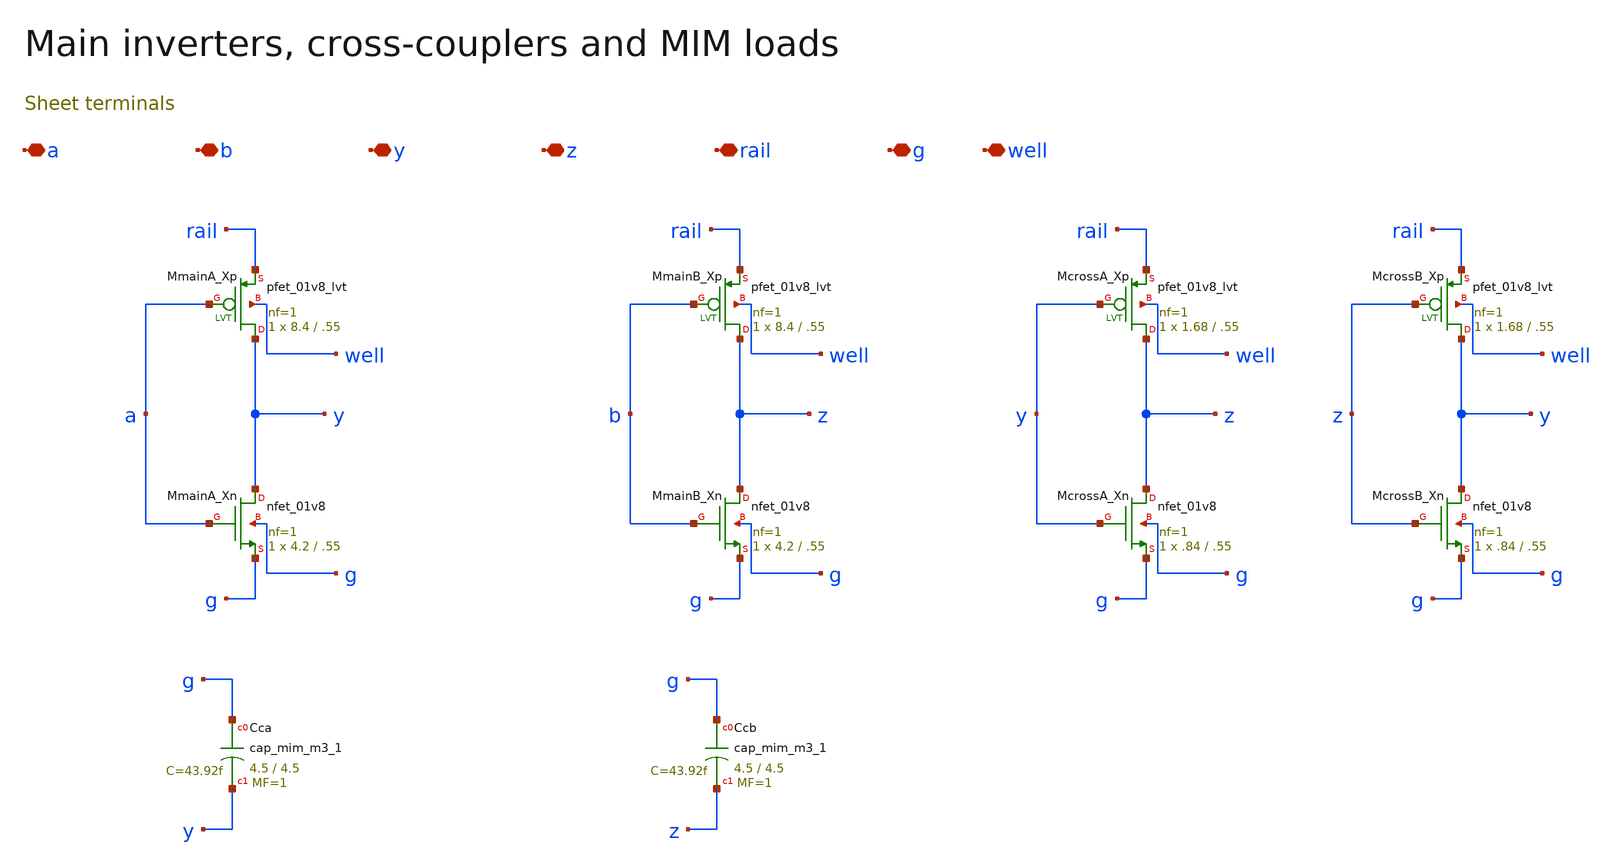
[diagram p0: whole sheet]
** sch_path: review/xschem/stage.sch
**.subckt stage a b y z rail g well
*.iopin a
*.iopin b
*.iopin y
*.iopin z
*.iopin rail
*.iopin g
*.iopin well
XCca g y sky130_fd_pr__cap_mim_m3_1 W=4.5 L=4.5 MF=1 m=1
XCcb g z sky130_fd_pr__cap_mim_m3_1 W=4.5 L=4.5 MF=1 m=1
XMmainA_Xp y a rail well sky130_fd_pr__pfet_01v8_lvt L=.55 W=8.4 nf=1 ad='int((1 + 1)/2) * 8.4 / 1 * 0.29'
+ as='int((1 + 2)/2) * 8.4 / 1 * 0.29' pd='2*int((1 + 1)/2) * (8.4 / 1 + 0.29)' ps='2*int((1 + 2)/2) * (8.4 / 1 + 0.29)'
+ nrd='0.29 / 8.4 ' nrs='0.29 / 8.4 ' sa=0 sb=0 sd=0 mult=1 m=1
XMmainA_Xn y a g g sky130_fd_pr__nfet_01v8 L=.55 W=4.2 nf=1 ad='int((1 + 1)/2) * 4.2 / 1 * 0.29' as='int((1 + 2)/2) * 4.2 / 1 * 0.29'
+ pd='2*int((1 + 1)/2) * (4.2 / 1 + 0.29)' ps='2*int((1 + 2)/2) * (4.2 / 1 + 0.29)' nrd='0.29 / 4.2 ' nrs='0.29 / 4.2 '
+ sa=0 sb=0 sd=0 mult=1 m=1
XMmainB_Xp z b rail well sky130_fd_pr__pfet_01v8_lvt L=.55 W=8.4 nf=1 ad='int((1 + 1)/2) * 8.4 / 1 * 0.29'
+ as='int((1 + 2)/2) * 8.4 / 1 * 0.29' pd='2*int((1 + 1)/2) * (8.4 / 1 + 0.29)' ps='2*int((1 + 2)/2) * (8.4 / 1 + 0.29)'
+ nrd='0.29 / 8.4 ' nrs='0.29 / 8.4 ' sa=0 sb=0 sd=0 mult=1 m=1
XMmainB_Xn z b g g sky130_fd_pr__nfet_01v8 L=.55 W=4.2 nf=1 ad='int((1 + 1)/2) * 4.2 / 1 * 0.29' as='int((1 + 2)/2) * 4.2 / 1 * 0.29'
+ pd='2*int((1 + 1)/2) * (4.2 / 1 + 0.29)' ps='2*int((1 + 2)/2) * (4.2 / 1 + 0.29)' nrd='0.29 / 4.2 ' nrs='0.29 / 4.2 '
+ sa=0 sb=0 sd=0 mult=1 m=1
XMcrossA_Xp z y rail well sky130_fd_pr__pfet_01v8_lvt L=.55 W=1.68 nf=1 ad='int((1 + 1)/2) * 1.68 / 1 * 0.29'
+ as='int((1 + 2)/2) * 1.68 / 1 * 0.29' pd='2*int((1 + 1)/2) * (1.68 / 1 + 0.29)' ps='2*int((1 + 2)/2) * (1.68 / 1 + 0.29)'
+ nrd='0.29 / 1.68 ' nrs='0.29 / 1.68 ' sa=0 sb=0 sd=0 mult=1 m=1
XMcrossA_Xn z y g g sky130_fd_pr__nfet_01v8 L=.55 W=.84 nf=1 ad='int((1 + 1)/2) * .84 / 1 * 0.29' as='int((1 + 2)/2) * .84 / 1 * 0.29'
+ pd='2*int((1 + 1)/2) * (.84 / 1 + 0.29)' ps='2*int((1 + 2)/2) * (.84 / 1 + 0.29)' nrd='0.29 / .84 ' nrs='0.29 / .84 '
+ sa=0 sb=0 sd=0 mult=1 m=1
XMcrossB_Xp y z rail well sky130_fd_pr__pfet_01v8_lvt L=.55 W=1.68 nf=1 ad='int((1 + 1)/2) * 1.68 / 1 * 0.29'
+ as='int((1 + 2)/2) * 1.68 / 1 * 0.29' pd='2*int((1 + 1)/2) * (1.68 / 1 + 0.29)' ps='2*int((1 + 2)/2) * (1.68 / 1 + 0.29)'
+ nrd='0.29 / 1.68 ' nrs='0.29 / 1.68 ' sa=0 sb=0 sd=0 mult=1 m=1
XMcrossB_Xn y z g g sky130_fd_pr__nfet_01v8 L=.55 W=.84 nf=1 ad='int((1 + 1)/2) * .84 / 1 * 0.29' as='int((1 + 2)/2) * .84 / 1 * 0.29'
+ pd='2*int((1 + 1)/2) * (.84 / 1 + 0.29)' ps='2*int((1 + 2)/2) * (.84 / 1 + 0.29)' nrd='0.29 / .84 ' nrs='0.29 / .84 '
+ sa=0 sb=0 sd=0 mult=1 m=1
**.ends
.end
